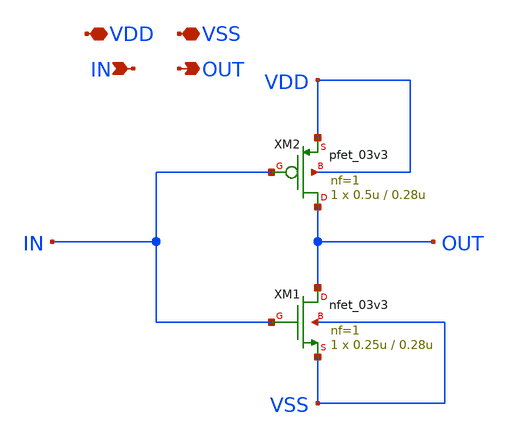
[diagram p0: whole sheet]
** sch_path: DAC_PAKISTAN_01/Pakistan1_Xschem/Inverter.sch
**.subckt Inverter VDD VSS IN OUT
*.iopin VDD
*.iopin VSS
*.ipin IN
*.opin OUT
XM1 OUT IN VSS VSS nfet_03v3 L=0.28u W=0.25u nf=1 ad='int((nf+1)/2) * W/nf * 0.18u' as='int((nf+2)/2) * W/nf * 0.18u'
+ pd='2*int((nf+1)/2) * (W/nf + 0.18u)' ps='2*int((nf+2)/2) * (W/nf + 0.18u)' nrd='0.18u / W' nrs='0.18u / W'
+ sa=0 sb=0 sd=0 m=1
XM2 OUT IN VDD VDD pfet_03v3 L=0.28u W=0.5u nf=1 ad='int((nf+1)/2) * W/nf * 0.18u' as='int((nf+2)/2) * W/nf * 0.18u'
+ pd='2*int((nf+1)/2) * (W/nf + 0.18u)' ps='2*int((nf+2)/2) * (W/nf + 0.18u)' nrd='0.18u / W' nrs='0.18u / W'
+ sa=0 sb=0 sd=0 m=1
**.ends
.end
